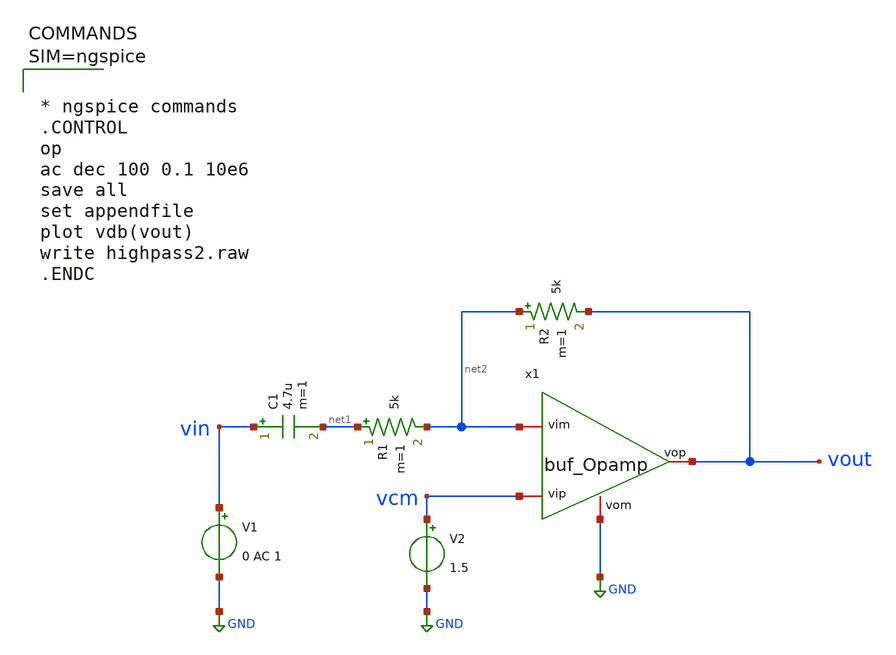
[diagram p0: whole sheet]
** sch_path: work/xschem/highpass2.sch
**.subckt highpass2
V1 vin GND 0 AC 1
R1 net1 net2 5k m=1
C1 vin net1 4.7u m=1
V2 vcm GND 1.5
R2 net2 vout 5k m=1
x1 vout vcm net2 GND buf_Opamp
**** begin user architecture code



* ngspice commands
.CONTROL
op
ac dec 100 0.1 10e6
save all
set appendfile
plot vdb(vout)
write highpass2.raw
.ENDC



**** end user architecture code
**.ends

* expanding   symbol:  buf_Opamp.sym # of pins=4
** sym_path: work/xschem/buf_Opamp.sym
** sch_path: work/xschem/buf_Opamp.sch
.subckt buf_Opamp vop vip vim vom
*.iopin vop
*.iopin vom
*.iopin vim
*.iopin vip
E1 net2 GND vip vim 1000
E2 vop vom net1 GND 1
R1 net2 net1 15.9k m=1
C1 net1 GND 10n m=1
.ends

.GLOBAL GND
.end
